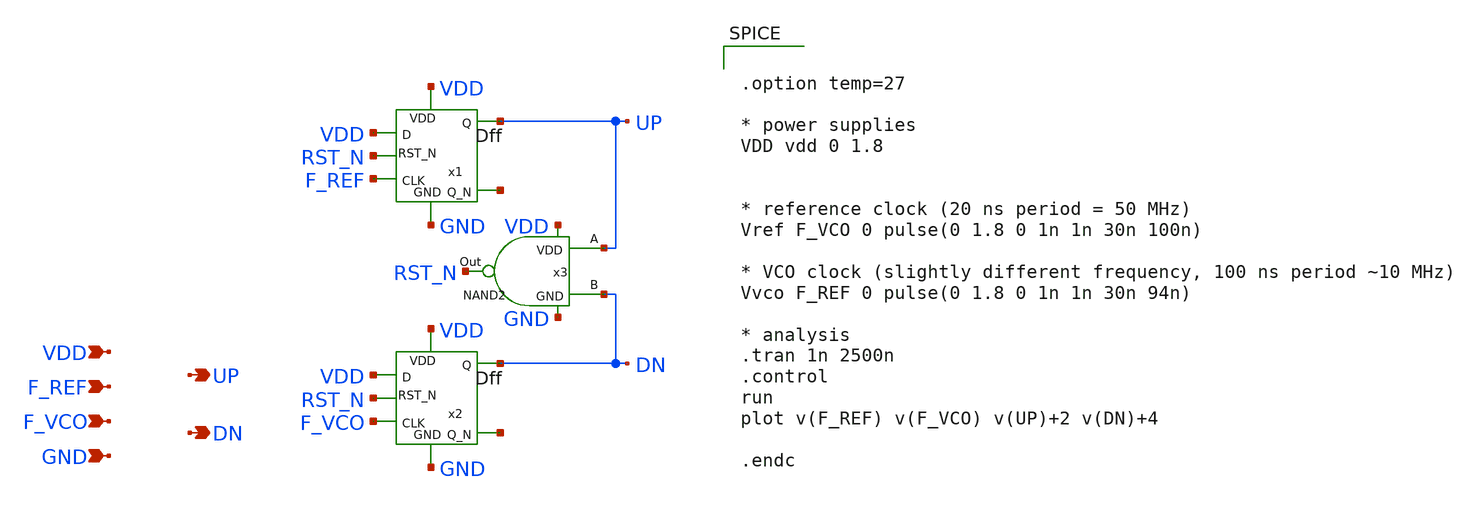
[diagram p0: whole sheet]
** sch_path: src/PFD_Dff.sch
* src/Dff.sym:
* Copyright 2022 Stefan Frederik Schippers
* Licensed under the Apache License, Version 2.0 (the "License");
**.subckt PFD_Dff UP F_REF VDD GND DN F_VCO
*.opin UP
*.ipin F_REF
*.ipin VDD
*.ipin GND
*.opin DN
*.ipin F_VCO
x1 VDD VDD GND F_REF UP net1 RST_N Dff
x2 VDD VDD GND F_VCO DN net2 RST_N Dff
x3 UP RST_N DN VDD GND NAND2
**** begin user architecture code

** opencircuitdesign pdks install
.lib $::SKYWATER_MODELS/sky130.lib.spice tt




.option temp=27

* power supplies
VDD vdd 0 1.8


* reference clock (20 ns period = 50 MHz)
Vref F_VCO 0 pulse(0 1.8 0 1n 1n 30n 100n)

* VCO clock (slightly different frequency, 100 ns period ~10 MHz)
Vvco F_REF 0 pulse(0 1.8 0 1n 1n 30n 94n)

* analysis
.tran 1n 2500n
.control
run
plot v(F_REF) v(F_VCO) v(UP)+2 v(DN)+4

.endc


**** end user architecture code
**.ends

* expanding   symbol:  /foss/designs/PLL2_4/src/Dff.sym # of pins=7
** sym_path: src/Dff.sym
** sch_path: src/Dff.sch
.subckt Dff D VDD GND CLK Q Q_N RST_N
*.opin Q
*.ipin D
*.ipin CLK
*.ipin VDD
*.ipin GND
*.opin Q_N
*.ipin RST_N
x3 VDD net3 D_n CLK net2 GND RST_N SR_NAND2
x4 VDD Q net2 net1 Q_N GND RST_N SR_NAND2
x5 net2 net1 D_n VDD GND CLK NAND3
x1 net1 D_n D VDD GND RST_N NAND3
.ends


* expanding   symbol:  /foss/designs/PLL2_4/src/NAND2.sym # of pins=5
** sym_path: src/NAND2.sym
** sch_path: src/NAND2.sch
.subckt NAND2 A Out B VDD GND
*.opin Out
*.ipin A
*.ipin B
*.ipin VDD
*.ipin GND
XM1 Out A VDD VDD sky130_fd_pr__pfet_01v8 L=1 W=1 nf=1 ad='int((1 + 1)/2) * 1 / 1 * 0.29' as='int((1 + 2)/2) * 1 / 1 * 0.29'
+ pd='2*int((1 + 1)/2) * (1 / 1 + 0.29)' ps='2*int((1 + 2)/2) * (1 / 1 + 0.29)' nrd='0.29 / 1 ' nrs='0.29 / 1 '
+ sa=0 sb=0 sd=0 mult=1 m=1
XM3 Out B VDD VDD sky130_fd_pr__pfet_01v8 L=1 W=1 nf=1 ad='int((1 + 1)/2) * 1 / 1 * 0.29' as='int((1 + 2)/2) * 1 / 1 * 0.29'
+ pd='2*int((1 + 1)/2) * (1 / 1 + 0.29)' ps='2*int((1 + 2)/2) * (1 / 1 + 0.29)' nrd='0.29 / 1 ' nrs='0.29 / 1 '
+ sa=0 sb=0 sd=0 mult=1 m=1
XM4 net1 B GND GND sky130_fd_pr__nfet_01v8 L=1 W=1 nf=1 ad='int((1 + 1)/2) * 1 / 1 * 0.29' as='int((1 + 2)/2) * 1 / 1 * 0.29'
+ pd='2*int((1 + 1)/2) * (1 / 1 + 0.29)' ps='2*int((1 + 2)/2) * (1 / 1 + 0.29)' nrd='0.29 / 1 ' nrs='0.29 / 1 '
+ sa=0 sb=0 sd=0 mult=1 m=1
XM5 Out A net1 GND sky130_fd_pr__nfet_01v8 L=1 W=1 nf=1 ad='int((1 + 1)/2) * 1 / 1 * 0.29' as='int((1 + 2)/2) * 1 / 1 * 0.29'
+ pd='2*int((1 + 1)/2) * (1 / 1 + 0.29)' ps='2*int((1 + 2)/2) * (1 / 1 + 0.29)' nrd='0.29 / 1 ' nrs='0.29 / 1 '
+ sa=0 sb=0 sd=0 mult=1 m=1
.ends


* expanding   symbol:  /foss/designs/PLL2_4/src/SR_NAND2.sym # of pins=7
** sym_path: src/SR_NAND2.sym
** sch_path: src/SR_NAND2.sch
.subckt SR_NAND2 VDD Q R S nQ GND RST_N
*.opin Q
*.ipin R
*.ipin S
*.ipin VDD
*.ipin GND
*.opin nQ
*.ipin RST_N
x2 R Q nQ VDD GND NAND2
x1 Q nQ S VDD GND RST_N NAND3
.ends


* expanding   symbol:  /foss/designs/PLL2_4/src/NAND3.sym # of pins=6
** sym_path: src/NAND3.sym
** sch_path: src/NAND3.sch
.subckt NAND3 A Out C VDD GND B
*.opin Out
*.ipin A
*.ipin B
*.ipin VDD
*.ipin GND
*.ipin C
XM1 Out A VDD VDD sky130_fd_pr__pfet_01v8 L=1 W=1 nf=1 ad='int((1 + 1)/2) * 1 / 1 * 0.29' as='int((1 + 2)/2) * 1 / 1 * 0.29'
+ pd='2*int((1 + 1)/2) * (1 / 1 + 0.29)' ps='2*int((1 + 2)/2) * (1 / 1 + 0.29)' nrd='0.29 / 1 ' nrs='0.29 / 1 '
+ sa=0 sb=0 sd=0 mult=1 m=1
XM3 Out C VDD VDD sky130_fd_pr__pfet_01v8 L=1 W=1 nf=1 ad='int((1 + 1)/2) * 1 / 1 * 0.29' as='int((1 + 2)/2) * 1 / 1 * 0.29'
+ pd='2*int((1 + 1)/2) * (1 / 1 + 0.29)' ps='2*int((1 + 2)/2) * (1 / 1 + 0.29)' nrd='0.29 / 1 ' nrs='0.29 / 1 '
+ sa=0 sb=0 sd=0 mult=1 m=1
XM4 net2 C GND GND sky130_fd_pr__nfet_01v8 L=1 W=1 nf=1 ad='int((1 + 1)/2) * 1 / 1 * 0.29' as='int((1 + 2)/2) * 1 / 1 * 0.29'
+ pd='2*int((1 + 1)/2) * (1 / 1 + 0.29)' ps='2*int((1 + 2)/2) * (1 / 1 + 0.29)' nrd='0.29 / 1 ' nrs='0.29 / 1 '
+ sa=0 sb=0 sd=0 mult=1 m=1
XM5 Out A net1 GND sky130_fd_pr__nfet_01v8 L=1 W=1 nf=1 ad='int((1 + 1)/2) * 1 / 1 * 0.29' as='int((1 + 2)/2) * 1 / 1 * 0.29'
+ pd='2*int((1 + 1)/2) * (1 / 1 + 0.29)' ps='2*int((1 + 2)/2) * (1 / 1 + 0.29)' nrd='0.29 / 1 ' nrs='0.29 / 1 '
+ sa=0 sb=0 sd=0 mult=1 m=1
XM2 Out B VDD VDD sky130_fd_pr__pfet_01v8 L=1 W=1 nf=1 ad='int((1 + 1)/2) * 1 / 1 * 0.29' as='int((1 + 2)/2) * 1 / 1 * 0.29'
+ pd='2*int((1 + 1)/2) * (1 / 1 + 0.29)' ps='2*int((1 + 2)/2) * (1 / 1 + 0.29)' nrd='0.29 / 1 ' nrs='0.29 / 1 '
+ sa=0 sb=0 sd=0 mult=1 m=1
XM6 net1 B net2 GND sky130_fd_pr__nfet_01v8 L=1 W=1 nf=1 ad='int((1 + 1)/2) * 1 / 1 * 0.29' as='int((1 + 2)/2) * 1 / 1 * 0.29'
+ pd='2*int((1 + 1)/2) * (1 / 1 + 0.29)' ps='2*int((1 + 2)/2) * (1 / 1 + 0.29)' nrd='0.29 / 1 ' nrs='0.29 / 1 '
+ sa=0 sb=0 sd=0 mult=1 m=1
.ends

.end
